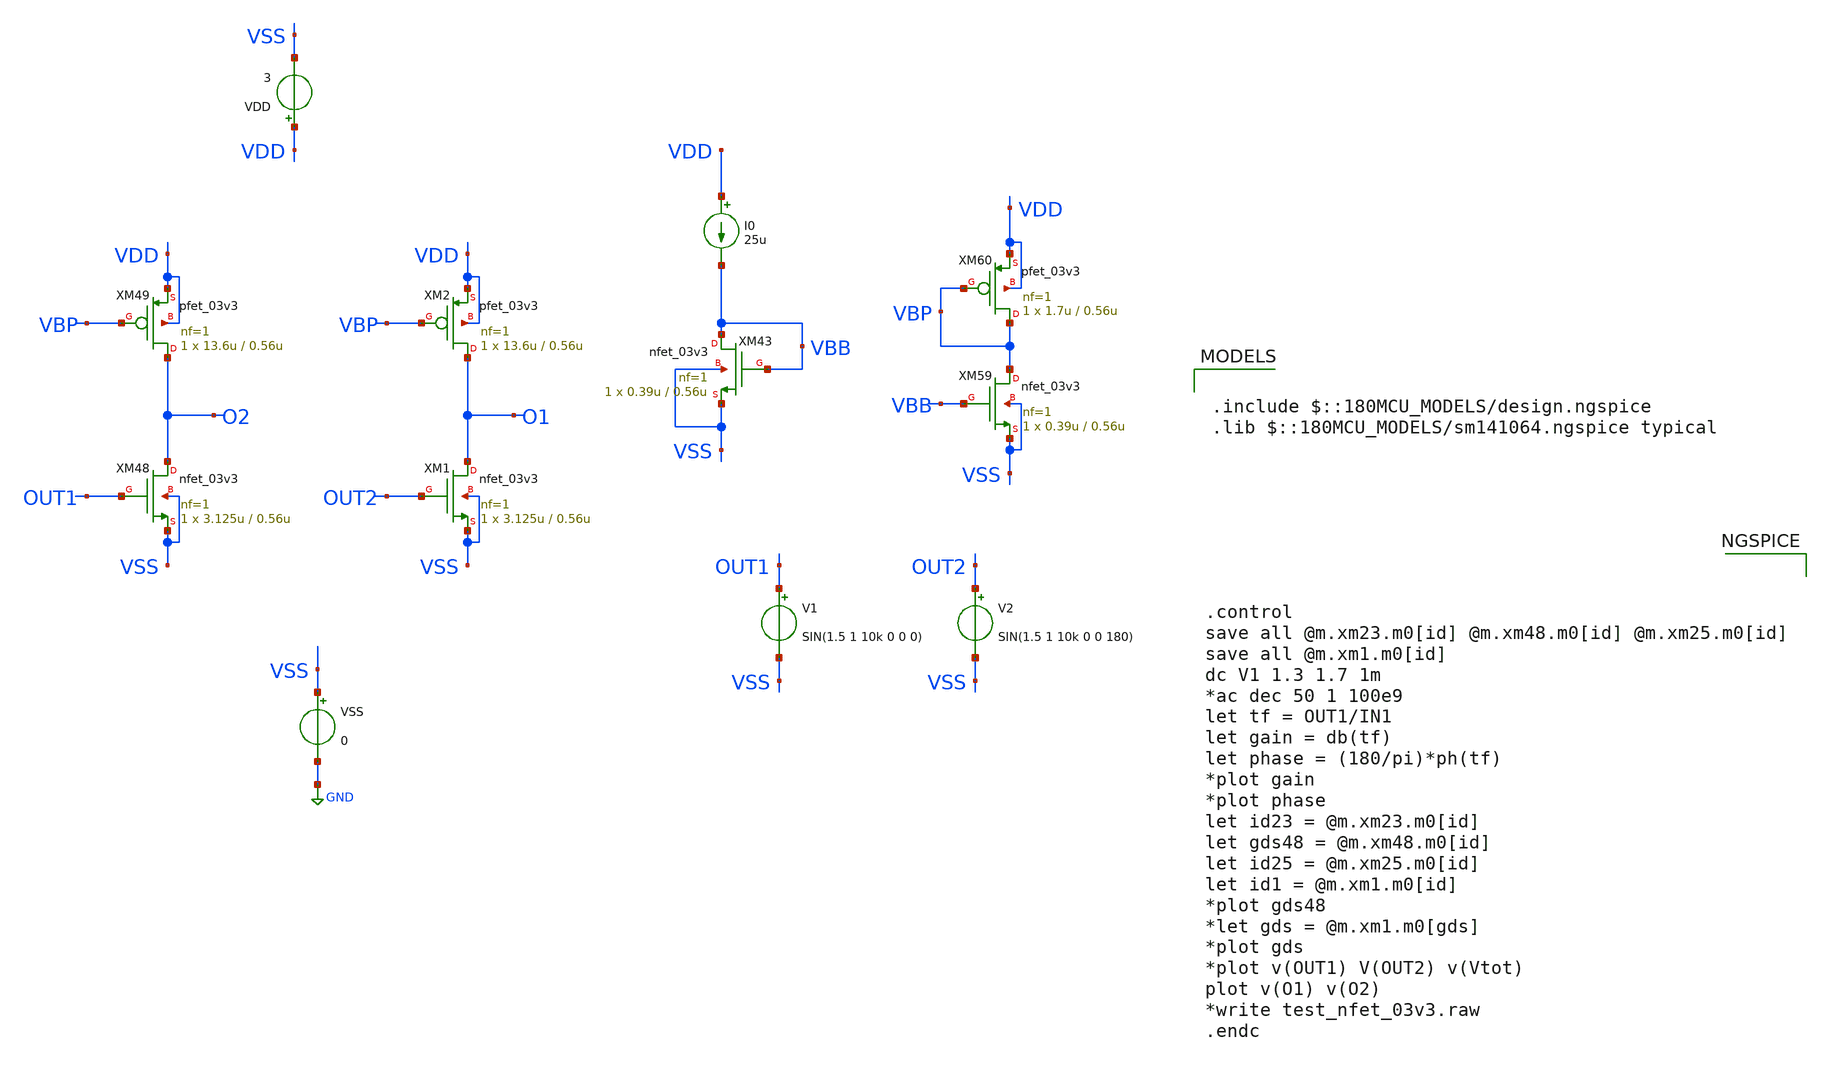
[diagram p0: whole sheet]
** sch_path: SCOP_INPUT_AND_MUX_PAKISTAN_03/Xschem/Others/PMOS_2nd.sch
**.subckt PMOS_2nd
XM48 O2 OUT1 VSS VSS nfet_03v3 L=0.56u W=3.125u nf=1 ad='int((nf+1)/2) * W/nf * 0.18u' as='int((nf+2)/2) * W/nf * 0.18u'
+ pd='2*int((nf+1)/2) * (W/nf + 0.18u)' ps='2*int((nf+2)/2) * (W/nf + 0.18u)' nrd='0.18u / W' nrs='0.18u / W'
+ sa=0 sb=0 sd=0 m=1
XM49 O2 VBP VDD VDD pfet_03v3 L=0.56u W=13.6u nf=1 ad='int((nf+1)/2) * W/nf * 0.18u' as='int((nf+2)/2) * W/nf * 0.18u'
+ pd='2*int((nf+1)/2) * (W/nf + 0.18u)' ps='2*int((nf+2)/2) * (W/nf + 0.18u)' nrd='0.18u / W' nrs='0.18u / W'
+ sa=0 sb=0 sd=0 m=1
XM1 O1 OUT2 VSS VSS nfet_03v3 L=0.56u W=3.125u nf=1 ad='int((nf+1)/2) * W/nf * 0.18u' as='int((nf+2)/2) * W/nf * 0.18u'
+ pd='2*int((nf+1)/2) * (W/nf + 0.18u)' ps='2*int((nf+2)/2) * (W/nf + 0.18u)' nrd='0.18u / W' nrs='0.18u / W'
+ sa=0 sb=0 sd=0 m=1
XM2 O1 VBP VDD VDD pfet_03v3 L=0.56u W=13.6u nf=1 ad='int((nf+1)/2) * W/nf * 0.18u' as='int((nf+2)/2) * W/nf * 0.18u'
+ pd='2*int((nf+1)/2) * (W/nf + 0.18u)' ps='2*int((nf+2)/2) * (W/nf + 0.18u)' nrd='0.18u / W' nrs='0.18u / W'
+ sa=0 sb=0 sd=0 m=1
XM43 VBB VBB VSS VSS nfet_03v3 L=0.56u W=0.39u nf=1 ad='int((nf+1)/2) * W/nf * 0.18u' as='int((nf+2)/2) * W/nf * 0.18u'
+ pd='2*int((nf+1)/2) * (W/nf + 0.18u)' ps='2*int((nf+2)/2) * (W/nf + 0.18u)' nrd='0.18u / W' nrs='0.18u / W'
+ sa=0 sb=0 sd=0 m=1
I0 VDD VBB 25u
XM59 VBP VBB VSS VSS nfet_03v3 L=0.56u W=0.39u nf=1 ad='int((nf+1)/2) * W/nf * 0.18u' as='int((nf+2)/2) * W/nf * 0.18u'
+ pd='2*int((nf+1)/2) * (W/nf + 0.18u)' ps='2*int((nf+2)/2) * (W/nf + 0.18u)' nrd='0.18u / W' nrs='0.18u / W'
+ sa=0 sb=0 sd=0 m=1
XM60 VBP VBP VDD VDD pfet_03v3 L=0.56u W=1.7u nf=1 ad='int((nf+1)/2) * W/nf * 0.18u' as='int((nf+2)/2) * W/nf * 0.18u'
+ pd='2*int((nf+1)/2) * (W/nf + 0.18u)' ps='2*int((nf+2)/2) * (W/nf + 0.18u)' nrd='0.18u / W' nrs='0.18u / W'
+ sa=0 sb=0 sd=0 m=1
V1 OUT1 VSS SIN(1.5 1 10k 0 0 0)
V2 OUT2 VSS SIN(1.5 1 10k 0 0 180)
VDD VDD VSS 3
VSS VSS GND 0
**** begin user architecture code

.include $::180MCU_MODELS/design.ngspice
.lib $::180MCU_MODELS/sm141064.ngspice typical




.control
save all @m.xm23.m0[id] @m.xm48.m0[id] @m.xm25.m0[id]
save all @m.xm1.m0[id]
dc V1 1.3 1.7 1m
*ac dec 50 1 100e9
let tf = OUT1/IN1
let gain = db(tf)
let phase = (180/pi)*ph(tf)
*plot gain
*plot phase
let id23 = @m.xm23.m0[id]
let gds48 = @m.xm48.m0[id]
let id25 = @m.xm25.m0[id]
let id1 = @m.xm1.m0[id]
*plot gds48
*let gds = @m.xm1.m0[gds]
*plot gds
*plot v(OUT1) V(OUT2) v(Vtot)
plot v(O1) v(O2)
*write test_nfet_03v3.raw
.endc


**** end user architecture code
**.ends
.GLOBAL GND
.end
